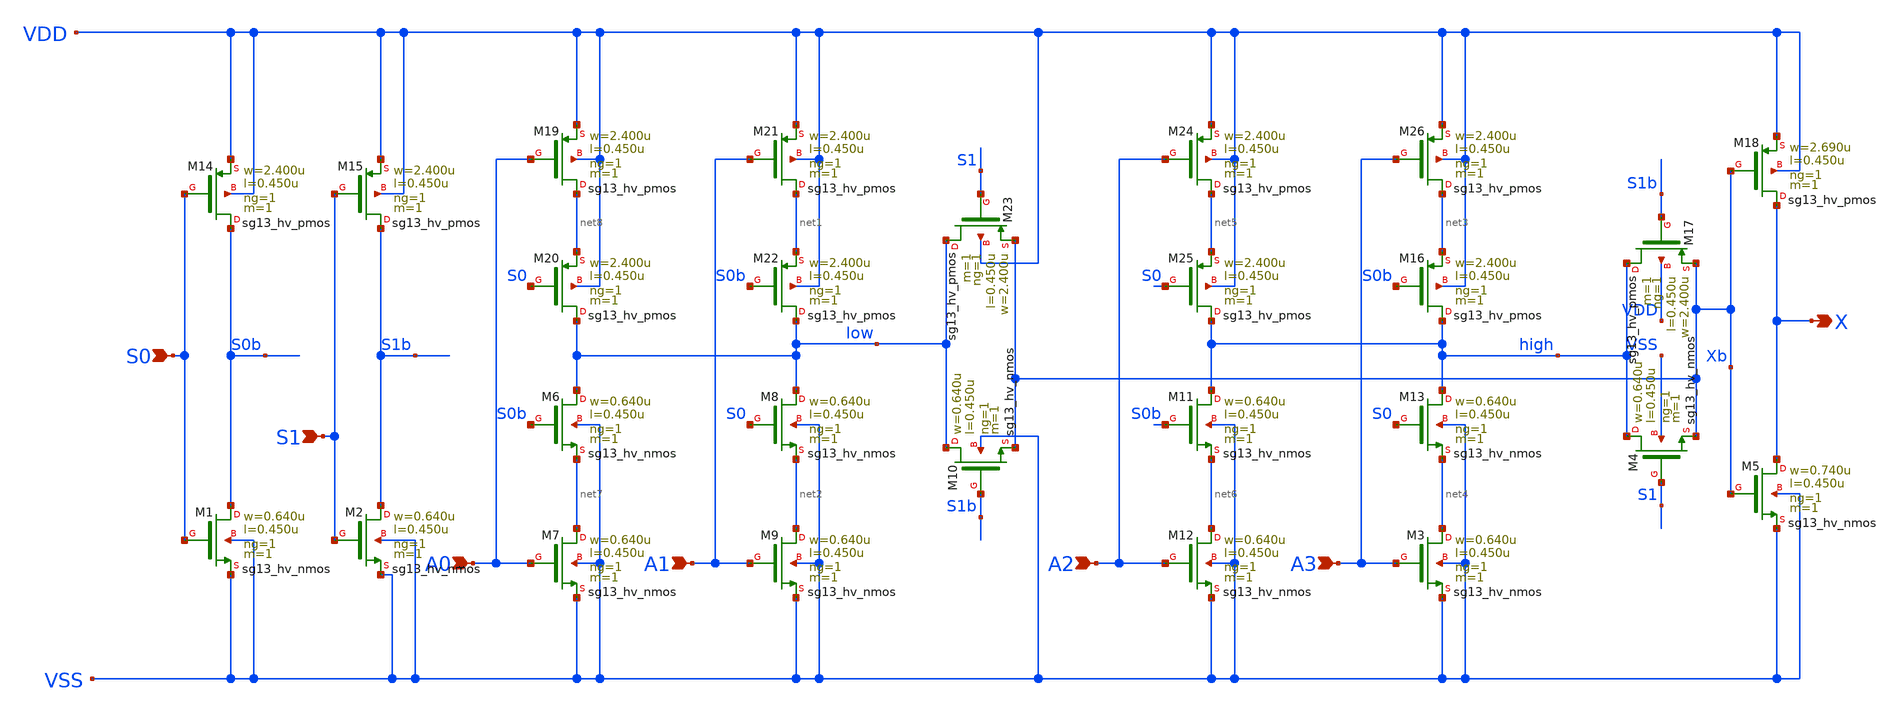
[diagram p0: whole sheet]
** sch_path: ihp-sg13g2/libs.ref/sg13g2_stdcell_hv/sch/xschem/sg13g2_hv_mux4_1.sch
* Copyright 2023 IHP PDK Authors
* Licensed under the Apache License, Version 2.0 (the "License");
* you may not use this file except in compliance with the License.
* You may obtain a copy of the License at
* https://www.apache.org/licenses/LICENSE-2.0
* Unless required by applicable law or agreed to in writing, software
* distributed under the License is distributed on an "AS IS" BASIS,
* WITHOUT WARRANTIES OR CONDITIONS OF ANY KIND, either express or implied.
* See the License for the specific language governing permissions and
* limitations under the License.
**.subckt sg13g2_hv_mux4_1 S0 S1 A0 A1 A2 A3 X
*.ipin S0
*.ipin S1
*.ipin A0
*.ipin A1
*.ipin A2
*.ipin A3
*.opin X
XM1 S0b S0 VSS VSS sg13_hv_nmos w=0.640u l=0.450u ng=1 m=1 mm_ok=1
XM2 S1b S1 VSS VSS sg13_hv_nmos w=0.640u l=0.450u ng=1 m=1 mm_ok=1
XM3 net4 A3 VSS VSS sg13_hv_nmos w=0.640u l=0.450u ng=1 m=1 mm_ok=1
XM4 high S1 Xb VSS sg13_hv_nmos w=0.640u l=0.450u ng=1 m=1 mm_ok=1
XM5 X Xb VSS VSS sg13_hv_nmos w=0.740u l=0.450u ng=1 m=1 mm_ok=1
XM6 low S0b net7 VSS sg13_hv_nmos w=0.640u l=0.450u ng=1 m=1 mm_ok=1
XM7 net7 A0 VSS VSS sg13_hv_nmos w=0.640u l=0.450u ng=1 m=1 mm_ok=1
XM8 low S0 net2 VSS sg13_hv_nmos w=0.640u l=0.450u ng=1 m=1 mm_ok=1
XM9 net2 A1 VSS VSS sg13_hv_nmos w=0.640u l=0.450u ng=1 m=1 mm_ok=1
XM10 low S1b Xb VSS sg13_hv_nmos w=0.640u l=0.450u ng=1 m=1 mm_ok=1
XM11 high S0b net6 VSS sg13_hv_nmos w=0.640u l=0.450u ng=1 m=1 mm_ok=1
XM12 net6 A2 VSS VSS sg13_hv_nmos w=0.640u l=0.450u ng=1 m=1 mm_ok=1
XM13 high S0 net4 VSS sg13_hv_nmos w=0.640u l=0.450u ng=1 m=1 mm_ok=1
XM14 S0b S0 VDD VDD sg13_hv_pmos w=2.400u l=0.450u ng=1 m=1 mm_ok=1
XM15 S1b S1 VDD VDD sg13_hv_pmos w=2.400u l=0.450u ng=1 m=1 mm_ok=1
XM16 high S0b net3 VDD sg13_hv_pmos w=2.400u l=0.450u ng=1 m=1 mm_ok=1
XM17 high S1b Xb VDD sg13_hv_pmos w=2.400u l=0.450u ng=1 m=1 mm_ok=1
XM18 X Xb VDD VDD sg13_hv_pmos w=2.690u l=0.450u ng=1 m=1 mm_ok=1
XM19 net8 A0 VDD VDD sg13_hv_pmos w=2.400u l=0.450u ng=1 m=1 mm_ok=1
XM20 low S0 net8 VDD sg13_hv_pmos w=2.400u l=0.450u ng=1 m=1 mm_ok=1
XM21 net1 A1 VDD VDD sg13_hv_pmos w=2.400u l=0.450u ng=1 m=1 mm_ok=1
XM22 low S0b net1 VDD sg13_hv_pmos w=2.400u l=0.450u ng=1 m=1 mm_ok=1
XM23 low S1 Xb VDD sg13_hv_pmos w=2.400u l=0.450u ng=1 m=1 mm_ok=1
XM24 net5 A2 VDD VDD sg13_hv_pmos w=2.400u l=0.450u ng=1 m=1 mm_ok=1
XM25 high S0 net5 VDD sg13_hv_pmos w=2.400u l=0.450u ng=1 m=1 mm_ok=1
XM26 net3 A3 VDD VDD sg13_hv_pmos w=2.400u l=0.450u ng=1 m=1 mm_ok=1
**.ends
.end
